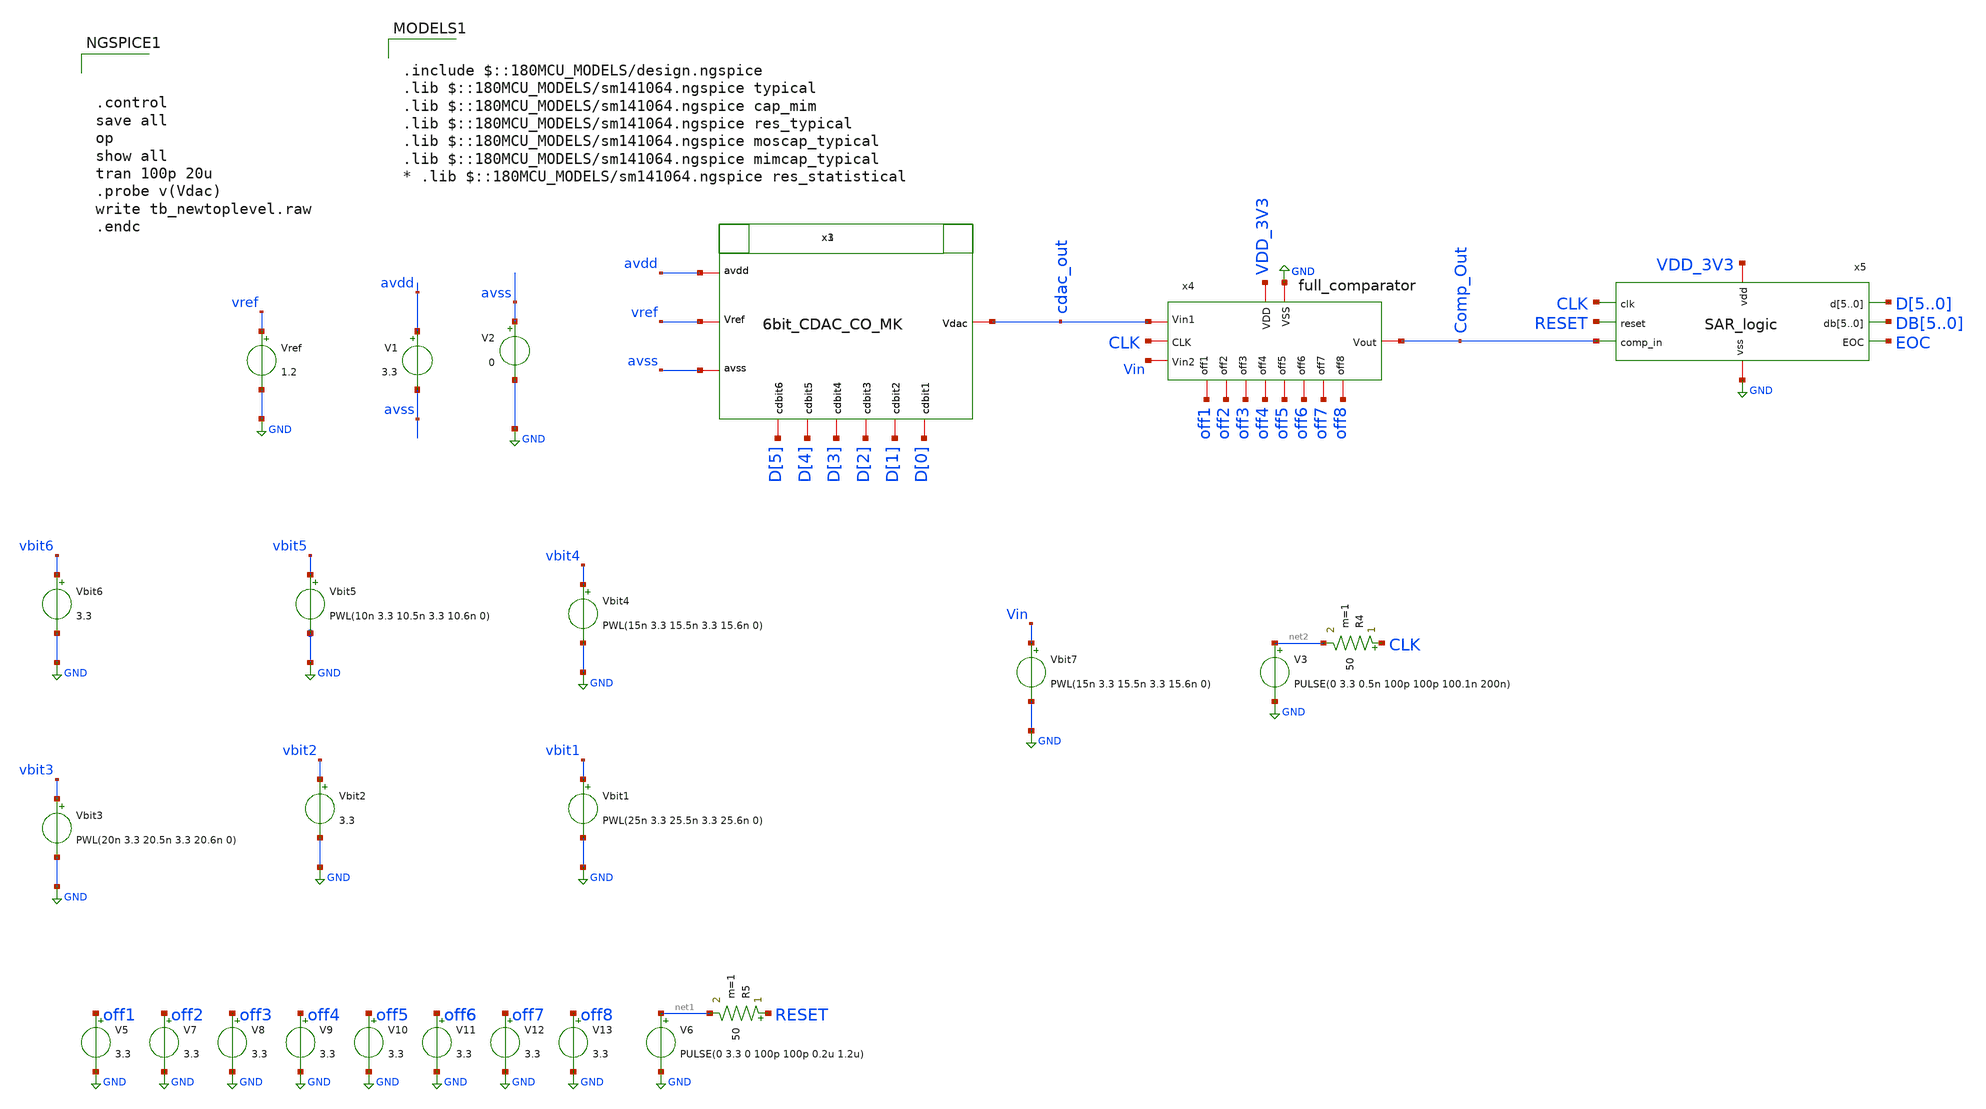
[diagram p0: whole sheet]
** sch_path: designs/full_ADC/tb_newtoplevel.sch
**.subckt tb_newtoplevel
V1 avdd avss 3.3
V2 avss GND 0
Vbit1 vbit1 GND PWL(25n 3.3 25.5n 3.3 25.6n 0)
Vbit2 vbit2 GND 3.3
Vbit3 vbit3 GND PWL(20n 3.3 20.5n 3.3 20.6n 0)
Vbit4 vbit4 GND PWL(15n 3.3 15.5n 3.3 15.6n 0)
Vbit5 vbit5 GND PWL(10n 3.3 10.5n 3.3 10.6n 0)
Vbit6 vbit6 GND 3.3
Vref vref GND 1.2
x1 cdac_out avdd avss vref D[5] D[4] D[2] D[0] D[1] D[3] 6bit_CDAC_CO_MK
x3 cdac_out avdd avss vref D[5] D[4] D[2] D[0] D[1] D[3] 6bit_CDAC_CO_MK
V5 off1 GND 3.3
V7 off2 GND 3.3
V8 off3 GND 3.3
V9 off4 GND 3.3
V10 off5 GND 3.3
V11 off6 GND 3.3
V12 off7 GND 3.3
V13 off8 GND 3.3
V6 net1 GND PULSE(0 3.3 0 100p 100p 0.2u 1.2u)
R5 RESET net1 50 m=1
x4 off1 VDD_3V3 GND off2 CLK off3 cdac_out off4 Vin off5 Comp_Out off6 off7 off8 full_comparator
x5 VDD_3V3 GND CLK RESET Comp_Out D5 D4 D3 D2 D1 D0 DB5 DB4 DB3 DB2 DB1 DB0 EOC SAR_logic
Vbit7 Vin GND PWL(15n 3.3 15.5n 3.3 15.6n 0)
V3 net2 GND PULSE(0 3.3 0.5n 100p 100p 100.1n 200n)
R4 CLK net2 50 m=1
**** begin user architecture code



.control
save all
op
show all
tran 100p 20u
.probe v(Vdac)
write tb_newtoplevel.raw
.endc



.include $::180MCU_MODELS/design.ngspice
.lib $::180MCU_MODELS/sm141064.ngspice typical
.lib $::180MCU_MODELS/sm141064.ngspice cap_mim
.lib $::180MCU_MODELS/sm141064.ngspice res_typical
.lib $::180MCU_MODELS/sm141064.ngspice moscap_typical
.lib $::180MCU_MODELS/sm141064.ngspice mimcap_typical
* .lib $::180MCU_MODELS/sm141064.ngspice res_statistical

**** end user architecture code
**.ends
.GLOBAL GND
.end
